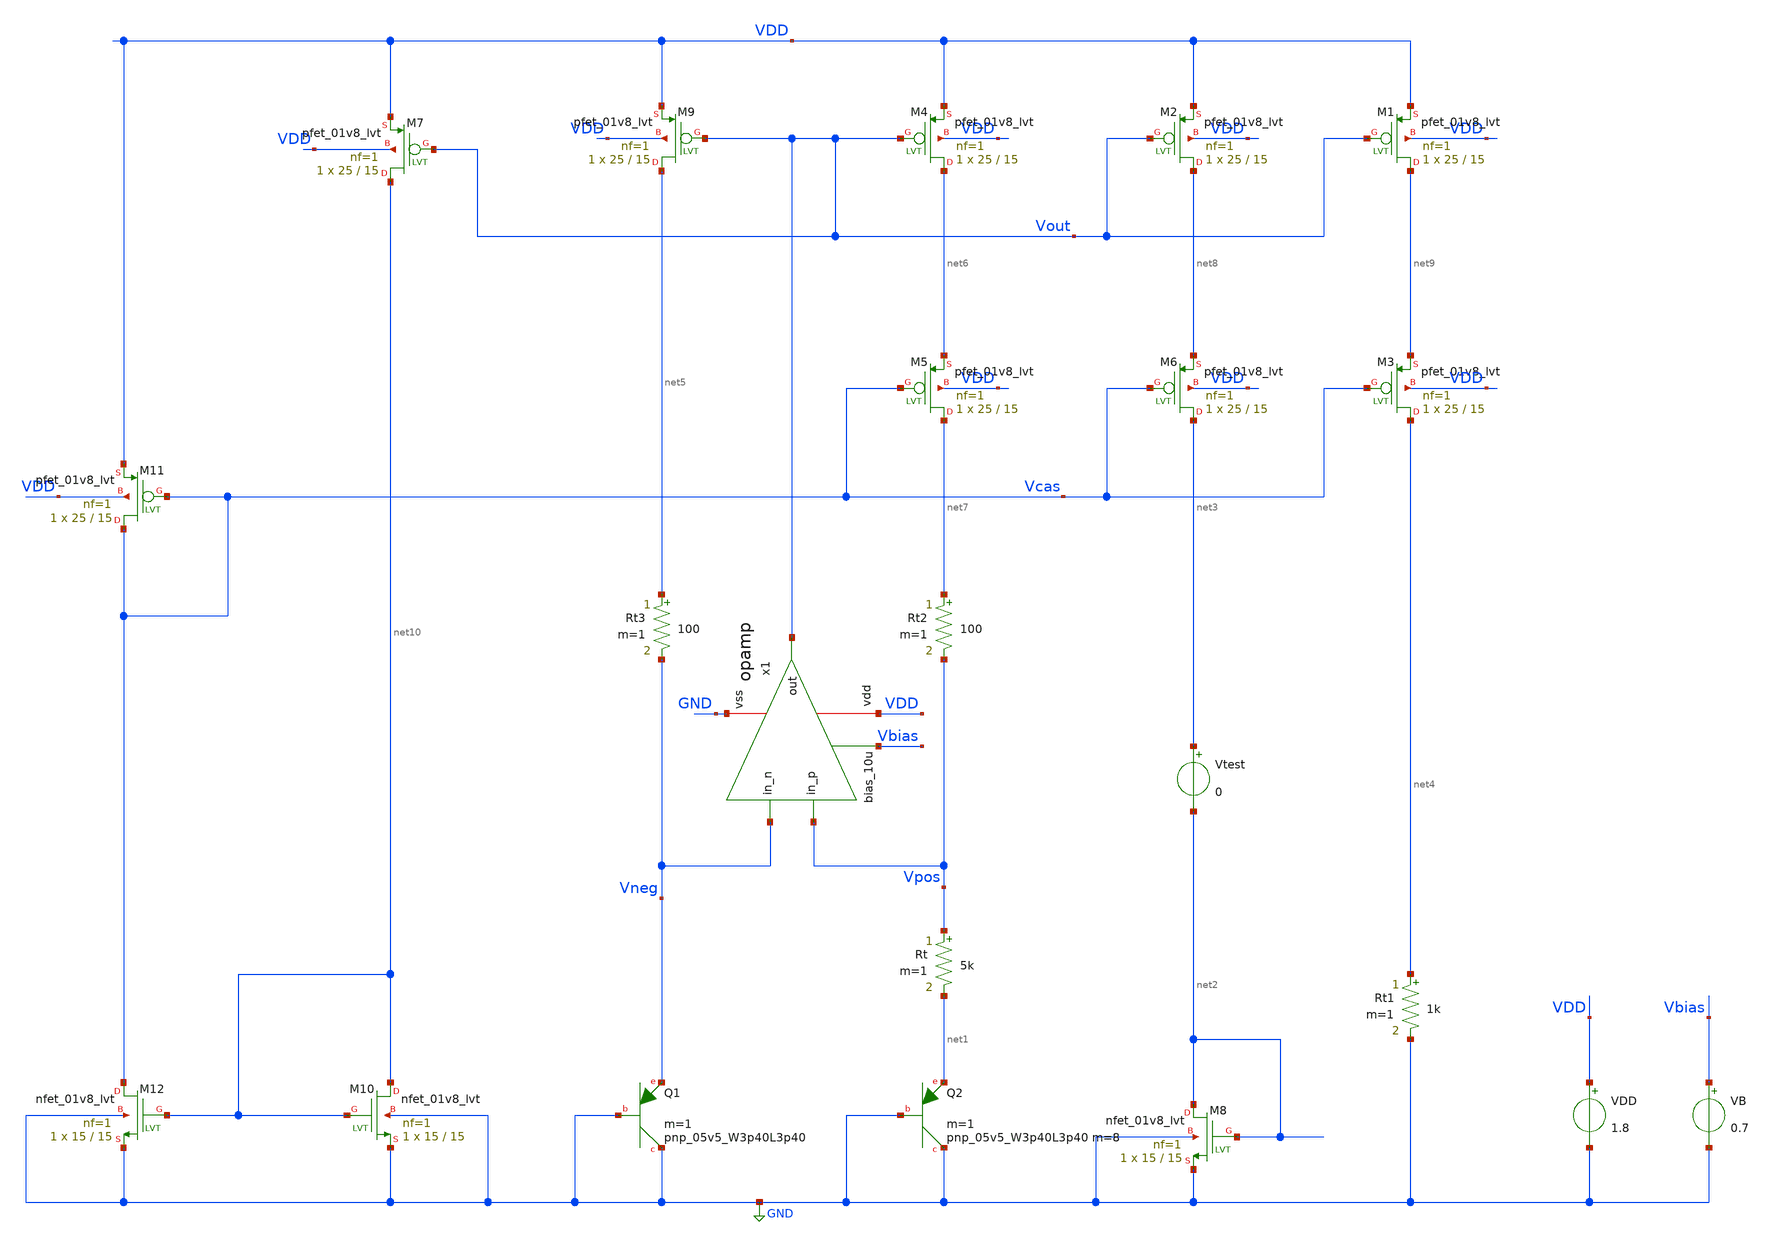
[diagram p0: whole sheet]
** sch_path: design/bgr_new/BGR.sch
**.subckt BGR
XQ1 GND GND Vneg sky130_fd_pr__pnp_05v5_W3p40L3p40 m=1
XQ2 GND GND net1 sky130_fd_pr__pnp_05v5_W3p40L3p40 m=8 m=1
XM8 net2 net2 GND GND sky130_fd_pr__nfet_01v8_lvt L=15 W=15 nf=1 ad='int((nf+1)/2) * W/nf * 0.29' as='int((nf+2)/2) * W/nf * 0.29'
+ pd='2*int((nf+1)/2) * (W/nf + 0.29)' ps='2*int((nf+2)/2) * (W/nf + 0.29)' nrd='0.29 / W' nrs='0.29 / W'
+ sa=0 sb=0 sd=0 mult=1 m=1
Vtest net3 net2 0
Rt1 net4 GND 1k m=1
Rt Vpos net1 5k m=1
VDD VDD GND 1.8
VB Vbias GND 0.7
XM3 net4 Vcas net9 VDD sky130_fd_pr__pfet_01v8_lvt L=15 W=25 nf=1 ad='int((nf+1)/2) * W * 0.29' as='int((nf+2)/2) * W * 0.29'
+ pd='2*int((nf+1)/2) * (W + 0.29)' ps='2*int((nf+2)/2) * (W + 0.29)' nrd='0.29 / W / nf' nrs='0.29 / W / nf'
+ sa=0 sb=0 sd=0 mult=1 m=1
XM10 net10 net10 GND GND sky130_fd_pr__nfet_01v8_lvt L=15 W=15 nf=1 ad='int((nf+1)/2) * W/nf * 0.29'
+ as='int((nf+2)/2) * W/nf * 0.29' pd='2*int((nf+1)/2) * (W/nf + 0.29)' ps='2*int((nf+2)/2) * (W/nf + 0.29)'
+ nrd='0.29 / W' nrs='0.29 / W' sa=0 sb=0 sd=0 mult=1 m=1
XM12 Vcas net10 GND GND sky130_fd_pr__nfet_01v8_lvt L=15 W=15 nf=1 ad='int((nf+1)/2) * W/nf * 0.29' as='int((nf+2)/2) * W/nf * 0.29'
+ pd='2*int((nf+1)/2) * (W/nf + 0.29)' ps='2*int((nf+2)/2) * (W/nf + 0.29)' nrd='0.29 / W' nrs='0.29 / W'
+ sa=0 sb=0 sd=0 mult=1 m=1
XM1 net9 Vout VDD VDD sky130_fd_pr__pfet_01v8_lvt L=15 W=25 nf=1 ad='int((nf+1)/2) * W * 0.29' as='int((nf+2)/2) * W * 0.29'
+ pd='2*int((nf+1)/2) * (W + 0.29)' ps='2*int((nf+2)/2) * (W + 0.29)' nrd='0.29 / W / nf' nrs='0.29 / W / nf'
+ sa=0 sb=0 sd=0 mult=1 m=1
XM2 net8 Vout VDD VDD sky130_fd_pr__pfet_01v8_lvt L=15 W=25 nf=1 ad='int((nf+1)/2) * W * 0.29' as='int((nf+2)/2) * W * 0.29'
+ pd='2*int((nf+1)/2) * (W + 0.29)' ps='2*int((nf+2)/2) * (W + 0.29)' nrd='0.29 / W / nf' nrs='0.29 / W / nf'
+ sa=0 sb=0 sd=0 mult=1 m=1
XM4 net6 Vout VDD VDD sky130_fd_pr__pfet_01v8_lvt L=15 W=25 nf=1 ad='int((nf+1)/2) * W * 0.29' as='int((nf+2)/2) * W * 0.29'
+ pd='2*int((nf+1)/2) * (W + 0.29)' ps='2*int((nf+2)/2) * (W + 0.29)' nrd='0.29 / W / nf' nrs='0.29 / W / nf'
+ sa=0 sb=0 sd=0 mult=1 m=1
XM5 net7 Vcas net6 VDD sky130_fd_pr__pfet_01v8_lvt L=15 W=25 nf=1 ad='int((nf+1)/2) * W * 0.29' as='int((nf+2)/2) * W * 0.29'
+ pd='2*int((nf+1)/2) * (W + 0.29)' ps='2*int((nf+2)/2) * (W + 0.29)' nrd='0.29 / W / nf' nrs='0.29 / W / nf'
+ sa=0 sb=0 sd=0 mult=1 m=1
XM6 net3 Vcas net8 VDD sky130_fd_pr__pfet_01v8_lvt L=15 W=25 nf=1 ad='int((nf+1)/2) * W * 0.29' as='int((nf+2)/2) * W * 0.29'
+ pd='2*int((nf+1)/2) * (W + 0.29)' ps='2*int((nf+2)/2) * (W + 0.29)' nrd='0.29 / W / nf' nrs='0.29 / W / nf'
+ sa=0 sb=0 sd=0 mult=1 m=1
XM7 net10 Vout VDD VDD sky130_fd_pr__pfet_01v8_lvt L=15 W=25 nf=1 ad='int((nf+1)/2) * W * 0.29' as='int((nf+2)/2) * W * 0.29'
+ pd='2*int((nf+1)/2) * (W + 0.29)' ps='2*int((nf+2)/2) * (W + 0.29)' nrd='0.29 / W / nf' nrs='0.29 / W / nf'
+ sa=0 sb=0 sd=0 mult=1 m=1
XM9 net5 Vout VDD VDD sky130_fd_pr__pfet_01v8_lvt L=15 W=25 nf=1 ad='int((nf+1)/2) * W * 0.29' as='int((nf+2)/2) * W * 0.29'
+ pd='2*int((nf+1)/2) * (W + 0.29)' ps='2*int((nf+2)/2) * (W + 0.29)' nrd='0.29 / W / nf' nrs='0.29 / W / nf'
+ sa=0 sb=0 sd=0 mult=1 m=1
XM11 Vcas Vcas VDD VDD sky130_fd_pr__pfet_01v8_lvt L=15 W=25 nf=1 ad='int((nf+1)/2) * W * 0.29' as='int((nf+2)/2) * W * 0.29'
+ pd='2*int((nf+1)/2) * (W + 0.29)' ps='2*int((nf+2)/2) * (W + 0.29)' nrd='0.29 / W / nf' nrs='0.29 / W / nf'
+ sa=0 sb=0 sd=0 mult=1 m=1
x1 VDD Vneg Vpos Vout Vbias GND opamp
Rt2 net7 Vpos 100 m=1
Rt3 net5 Vneg 100 m=1
**** begin user architecture code

** opencircuitdesign pdks install
.lib $::SKYWATER_MODELS/sky130.lib.spice tt_mm




.options savecurrents

*** plot vbgp with variation in supply voltage
*Vdd VDD GND 3.3
*V_en en GND 3.3
*.dc Vdd 2 4 0.1
*.control
*run
*print Vbgp
*plot V(Vbgp)
*.endc

*** plot vbgp with variation in temperature @3.3V
*Vdd VDD GND 3.3
*V_en en GND 3.3
*.dc temp -40 100 1 Rt 100 20k 1k
*.dc temp -40 100 1

.option
.control
let startR = 16k
let endR = 17k
let incre = 100
let curR = startR
while curR le endR
alter Rt curR
dc temp -40 100 1
write dc.out Vout
set appendwrite
let curR = curR + incre
end
run
*print V(VE)
*plot V(VE)
*plot deriv(V(VE))/1.202344
*plot V(Vout) V(Vcas) V(Vpos) V(Vneg)
*plot V(Vout)
*plot deriv(V(Vout))/1.202344

plot dc1.Vout dc2.Vout dc3.Vout dc4.Vout dc5.Vout dc6.Vout dc7.Vout dc8.Vout dc9.Vout dc10.Vout
*dc11.Vout dc12.Vout dc13.Vout dc14.Vout dc15.Vout

.endc

*** plot voltage coefficient
*Vdd VDD GND 3.3
*V_en en GND 3.3
*.dc Vdd 2 4 0.1
*.control
*run
*plot deriv(V(Vbgp))
*.endc

*** plot temperature coefficient
*Vdd VDD GND 3.3
*V_en en GND 3.3
*.dc temp -40 140 1
*.control
*run
*plot deriv(V(Vbgp))/1.202344
*.endc



*** enable pin
*Vdd VDD GND 3.3
*V_en en GND PULSE(0 3.3 0 200us 200us 600us 2000us 0)
*.tran 1u 2000us
*.control
*run
*plot V(en)
*plot -I(VDD)
*.endc


**** end user architecture code
**.ends

* expanding   symbol:  opamp/opamp.sym # of pins=6
** sym_path: design/opamp/opamp.sym
** sch_path: design/opamp/opamp.sch
.subckt opamp vdd in_n in_p out bias_10u vss
*.iopin vdd
*.iopin vss
*.ipin in_n
*.ipin in_p
*.opin out
*.ipin bias_10u
XM1 bias_10u bias_10u vss vss sky130_fd_pr__nfet_01v8_lvt L=2 W=1 nf=1 ad='int((nf+1)/2) * W/nf * 0.29'
+ as='int((nf+2)/2) * W/nf * 0.29' pd='2*int((nf+1)/2) * (W/nf + 0.29)' ps='2*int((nf+2)/2) * (W/nf + 0.29)'
+ nrd='0.29 / W' nrs='0.29 / W' sa=0 sb=0 sd=0 mult=1 m=1
XM_diff_n net3 in_n net1 vss sky130_fd_pr__nfet_01v8_lvt L=1 W=9 nf=1 ad='int((nf+1)/2) * W/nf * 0.29'
+ as='int((nf+2)/2) * W/nf * 0.29' pd='2*int((nf+1)/2) * (W/nf + 0.29)' ps='2*int((nf+2)/2) * (W/nf + 0.29)'
+ nrd='0.29 / W' nrs='0.29 / W' sa=0 sb=0 sd=0 mult=2 m=2
XM_diff_n1 net4 in_p net1 vss sky130_fd_pr__nfet_01v8_lvt L=1 W=9 nf=1 ad='int((nf+1)/2) * W/nf * 0.29'
+ as='int((nf+2)/2) * W/nf * 0.29' pd='2*int((nf+1)/2) * (W/nf + 0.29)' ps='2*int((nf+2)/2) * (W/nf + 0.29)'
+ nrd='0.29 / W' nrs='0.29 / W' sa=0 sb=0 sd=0 mult=2 m=2
XM_tail net1 net2 vss vss sky130_fd_pr__nfet_01v8_lvt L=4 W=5 nf=1 ad='int((nf+1)/2) * W/nf * 0.29' as='int((nf+2)/2) * W/nf * 0.29'
+ pd='2*int((nf+1)/2) * (W/nf + 0.29)' ps='2*int((nf+2)/2) * (W/nf + 0.29)' nrd='0.29 / W' nrs='0.29 / W'
+ sa=0 sb=0 sd=0 mult=8 m=8
XM_actload out net2 vss vss sky130_fd_pr__nfet_01v8_lvt L=2 W=4 nf=1 ad='int((nf+1)/2) * W/nf * 0.29'
+ as='int((nf+2)/2) * W/nf * 0.29' pd='2*int((nf+1)/2) * (W/nf + 0.29)' ps='2*int((nf+2)/2) * (W/nf + 0.29)'
+ nrd='0.29 / W' nrs='0.29 / W' sa=0 sb=0 sd=0 mult=6 m=6
XM_ppair_p net4 net3 vdd vdd sky130_fd_pr__pfet_01v8_lvt L=2 W=8 nf=1 ad='int((nf+1)/2) * W/nf * 0.29'
+ as='int((nf+2)/2) * W/nf * 0.29' pd='2*int((nf+1)/2) * (W/nf + 0.29)' ps='2*int((nf+2)/2) * (W/nf + 0.29)'
+ nrd='0.29 / W' nrs='0.29 / W' sa=0 sb=0 sd=0 mult=8 m=8
XM_ppair_p1 net3 net3 vdd vdd sky130_fd_pr__pfet_01v8_lvt L=2 W=8 nf=1 ad='int((nf+1)/2) * W/nf * 0.29'
+ as='int((nf+2)/2) * W/nf * 0.29' pd='2*int((nf+1)/2) * (W/nf + 0.29)' ps='2*int((nf+2)/2) * (W/nf + 0.29)'
+ nrd='0.29 / W' nrs='0.29 / W' sa=0 sb=0 sd=0 mult=8 m=8
XM_cs out net4 vdd vdd sky130_fd_pr__pfet_01v8_lvt L=0.5 W=12 nf=1 ad='int((nf+1)/2) * W/nf * 0.29' as='int((nf+2)/2) * W/nf * 0.29'
+ pd='2*int((nf+1)/2) * (W/nf + 0.29)' ps='2*int((nf+2)/2) * (W/nf + 0.29)' nrd='0.29 / W' nrs='0.29 / W'
+ sa=0 sb=0 sd=0 mult=12 m=12
V1 net2 vss 0.7
C1 net4 net5 150f m=1
R1 out net5 400 m=1
.ends

.GLOBAL GND
.end
